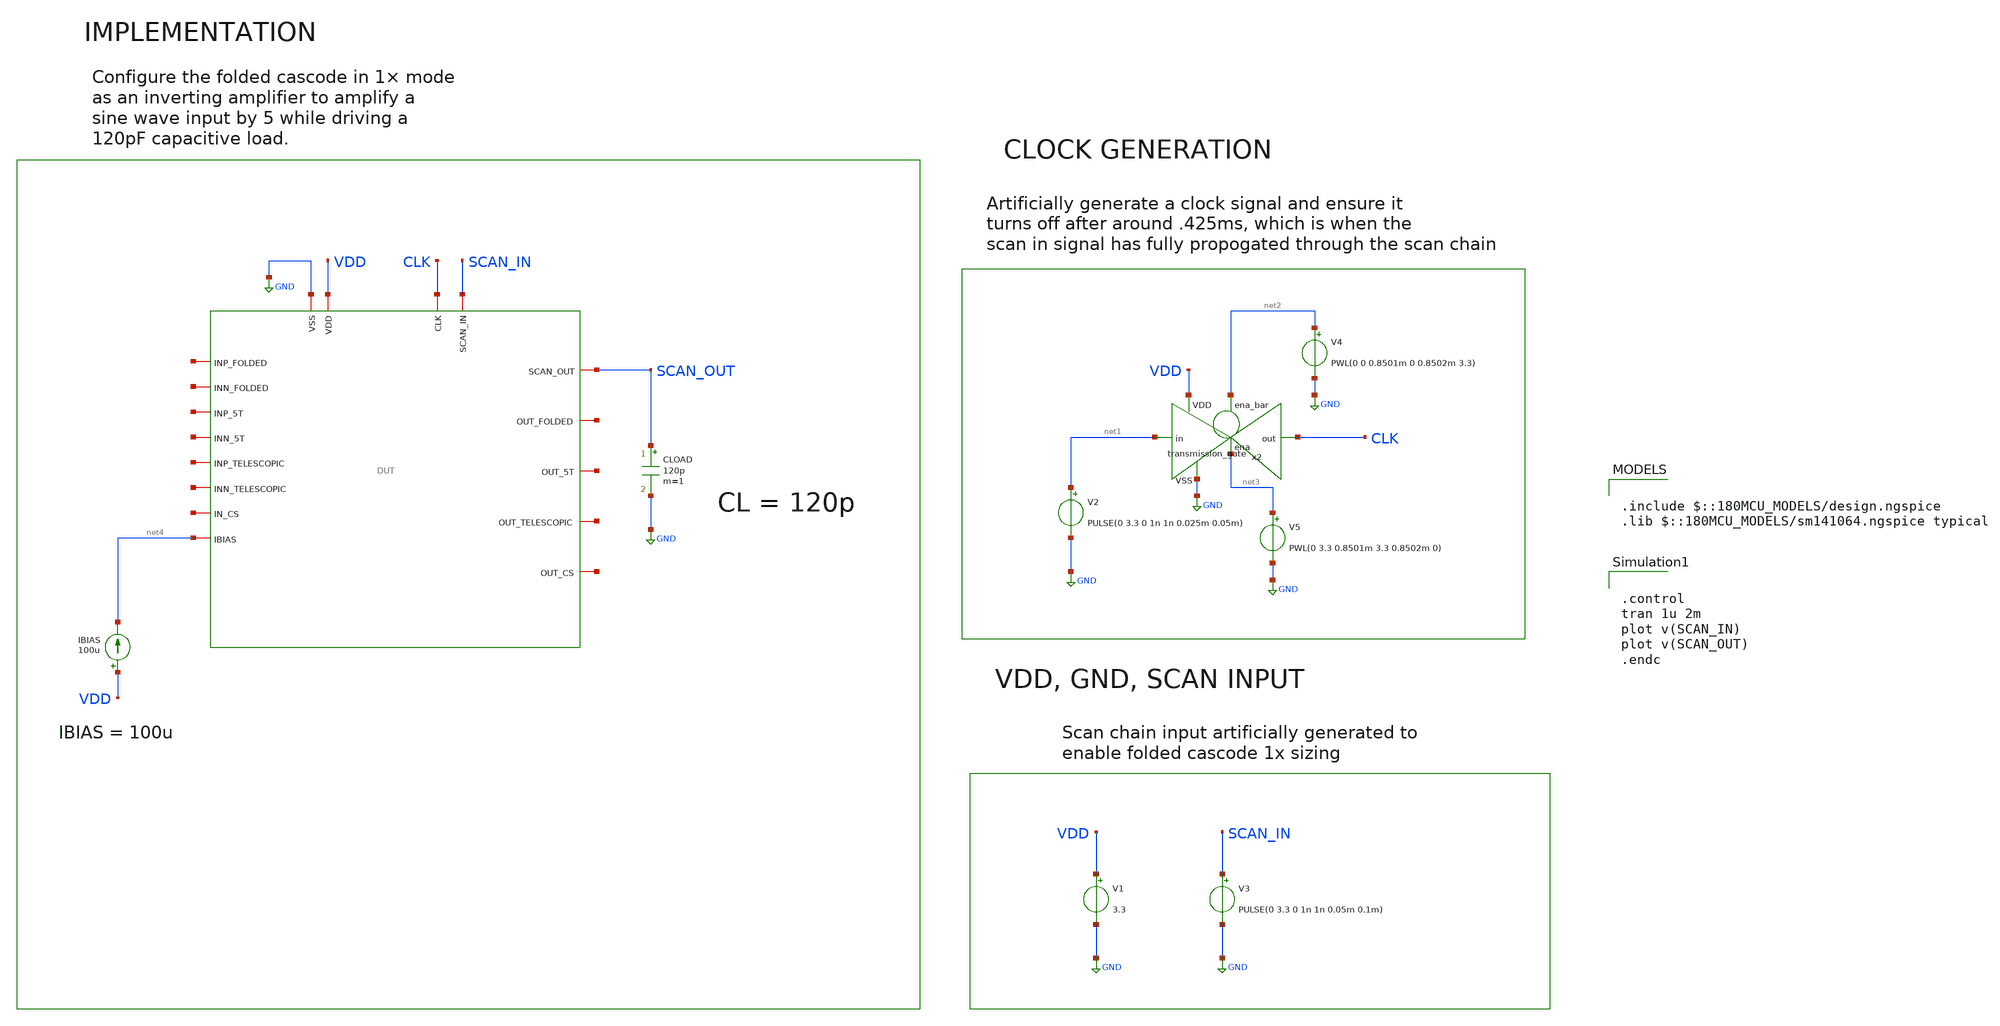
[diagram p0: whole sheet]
** sch_path: designs/libs/core_tb/mrd/tb_scan_out.sch
**.subckt tb_scan_out
V3 SCAN_IN GND PULSE(0 3.3 0 1n 1n 0.05m 0.1m)
V1 VDD GND 3.3
V2 net1 GND PULSE(0 3.3 0 1n 1n 0.025m 0.05m)
x2 net2 VDD CLK net1 GND net3 transmission_gate
V4 net2 GND PWL(0 0 0.8501m 0 0.8502m 3.3)
V5 net3 GND PWL(0 3.3 0.8501m 3.3 0.8502m 0)
IBIAS VDD net4 100u
CLOAD SCAN_OUT GND 120p m=1
x1 CLK SCAN_OUT SCAN_IN GND VDD net5 net6 net7 net4 net8 net9 net10 net11 net12 net13 net14 net15
+ DUT
**** begin user architecture code

.include $::180MCU_MODELS/design.ngspice
.lib $::180MCU_MODELS/sm141064.ngspice typical



.control
tran 1u 2m
plot v(SCAN_IN)
plot v(SCAN_OUT)
.endc


**** end user architecture code
**.ends
.GLOBAL GND
.end
